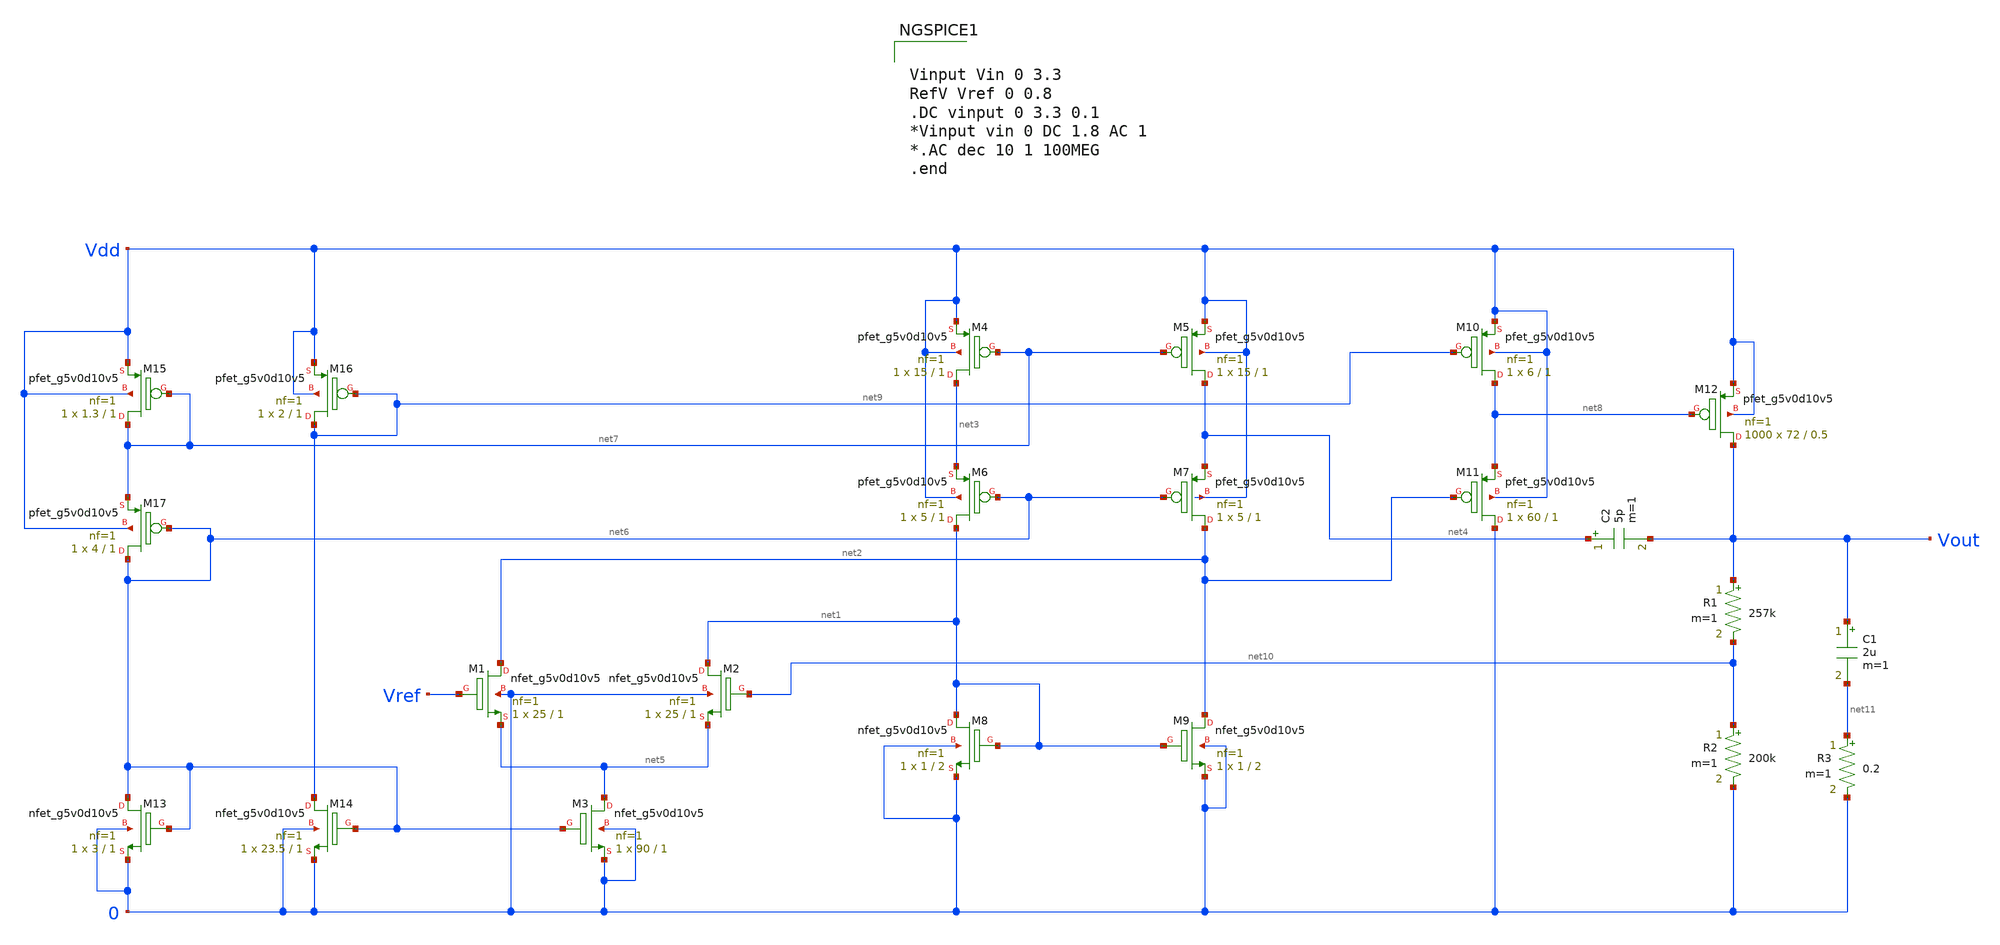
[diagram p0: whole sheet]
** sch_path: LDO/Schematic/LOw_Drop_LDO.sch
**.subckt LOw_Drop_LDO
XM1 net2 Vref net5 0 sky130_fd_pr__nfet_g5v0d10v5 L=1 W=25 nf=1 ad='int((nf+1)/2) * W/nf * 0.29' as='int((nf+2)/2) * W/nf * 0.29'
+ pd='2*int((nf+1)/2) * (W/nf + 0.29)' ps='2*int((nf+2)/2) * (W/nf + 0.29)' nrd='0.29 / W' nrs='0.29 / W'
+ sa=0 sb=0 sd=0 mult=1 m=1
XM2 net1 net10 net5 0 sky130_fd_pr__nfet_g5v0d10v5 L=1 W=25 nf=1 ad='int((nf+1)/2) * W/nf * 0.29' as='int((nf+2)/2) * W/nf * 0.29'
+ pd='2*int((nf+1)/2) * (W/nf + 0.29)' ps='2*int((nf+2)/2) * (W/nf + 0.29)' nrd='0.29 / W' nrs='0.29 / W'
+ sa=0 sb=0 sd=0 mult=1 m=1
XM3 net5 net6 0 0 sky130_fd_pr__nfet_g5v0d10v5 L=1 W=90 nf=1 ad='int((nf+1)/2) * W/nf * 0.29' as='int((nf+2)/2) * W/nf * 0.29'
+ pd='2*int((nf+1)/2) * (W/nf + 0.29)' ps='2*int((nf+2)/2) * (W/nf + 0.29)' nrd='0.29 / W' nrs='0.29 / W'
+ sa=0 sb=0 sd=0 mult=1 m=1
XM4 net3 net7 Vdd Vdd sky130_fd_pr__pfet_g5v0d10v5 L=1 W=15 nf=1 ad='int((nf+1)/2) * W/nf * 0.29' as='int((nf+2)/2) * W/nf * 0.29'
+ pd='2*int((nf+1)/2) * (W/nf + 0.29)' ps='2*int((nf+2)/2) * (W/nf + 0.29)' nrd='0.29 / W' nrs='0.29 / W'
+ sa=0 sb=0 sd=0 mult=1 m=1
XM5 net4 net7 Vdd Vdd sky130_fd_pr__pfet_g5v0d10v5 L=1 W=15 nf=1 ad='int((nf+1)/2) * W/nf * 0.29' as='int((nf+2)/2) * W/nf * 0.29'
+ pd='2*int((nf+1)/2) * (W/nf + 0.29)' ps='2*int((nf+2)/2) * (W/nf + 0.29)' nrd='0.29 / W' nrs='0.29 / W'
+ sa=0 sb=0 sd=0 mult=1 m=1
XM6 net1 net6 net3 Vdd sky130_fd_pr__pfet_g5v0d10v5 L=1 W=5 nf=1 ad='int((nf+1)/2) * W/nf * 0.29' as='int((nf+2)/2) * W/nf * 0.29'
+ pd='2*int((nf+1)/2) * (W/nf + 0.29)' ps='2*int((nf+2)/2) * (W/nf + 0.29)' nrd='0.29 / W' nrs='0.29 / W'
+ sa=0 sb=0 sd=0 mult=1 m=1
XM7 net2 net6 net4 Vdd sky130_fd_pr__pfet_g5v0d10v5 L=1 W=5 nf=1 ad='int((nf+1)/2) * W/nf * 0.29' as='int((nf+2)/2) * W/nf * 0.29'
+ pd='2*int((nf+1)/2) * (W/nf + 0.29)' ps='2*int((nf+2)/2) * (W/nf + 0.29)' nrd='0.29 / W' nrs='0.29 / W'
+ sa=0 sb=0 sd=0 mult=1 m=1
XM8 net1 net1 0 0 sky130_fd_pr__nfet_g5v0d10v5 L=2 W=1 nf=1 ad='int((nf+1)/2) * W/nf * 0.29' as='int((nf+2)/2) * W/nf * 0.29'
+ pd='2*int((nf+1)/2) * (W/nf + 0.29)' ps='2*int((nf+2)/2) * (W/nf + 0.29)' nrd='0.29 / W' nrs='0.29 / W'
+ sa=0 sb=0 sd=0 mult=1 m=1
XM9 net2 net1 0 0 sky130_fd_pr__nfet_g5v0d10v5 L=2 W=1 nf=1 ad='int((nf+1)/2) * W/nf * 0.29' as='int((nf+2)/2) * W/nf * 0.29'
+ pd='2*int((nf+1)/2) * (W/nf + 0.29)' ps='2*int((nf+2)/2) * (W/nf + 0.29)' nrd='0.29 / W' nrs='0.29 / W'
+ sa=0 sb=0 sd=0 mult=1 m=1
XM10 net8 net9 Vdd Vdd sky130_fd_pr__pfet_g5v0d10v5 L=1 W=6 nf=1 ad='int((nf+1)/2) * W/nf * 0.29' as='int((nf+2)/2) * W/nf * 0.29'
+ pd='2*int((nf+1)/2) * (W/nf + 0.29)' ps='2*int((nf+2)/2) * (W/nf + 0.29)' nrd='0.29 / W' nrs='0.29 / W'
+ sa=0 sb=0 sd=0 mult=1 m=1
XM11 0 net2 net8 Vdd sky130_fd_pr__pfet_g5v0d10v5 L=1 W=60 nf=1 ad='int((nf+1)/2) * W/nf * 0.29' as='int((nf+2)/2) * W/nf * 0.29'
+ pd='2*int((nf+1)/2) * (W/nf + 0.29)' ps='2*int((nf+2)/2) * (W/nf + 0.29)' nrd='0.29 / W' nrs='0.29 / W'
+ sa=0 sb=0 sd=0 mult=1 m=1
XM12 Vout net8 Vdd Vdd sky130_fd_pr__pfet_g5v0d10v5 L=0.5 W=72 nf=1 ad='int((nf+1)/2) * W/nf * 0.29'
+ as='int((nf+2)/2) * W/nf * 0.29' pd='2*int((nf+1)/2) * (W/nf + 0.29)' ps='2*int((nf+2)/2) * (W/nf + 0.29)'
+ nrd='0.29 / W' nrs='0.29 / W' sa=0 sb=0 sd=0 mult=1000 m=1000
XM13 net6 net6 0 0 sky130_fd_pr__nfet_g5v0d10v5 L=1 W=3 nf=1 ad='int((nf+1)/2) * W/nf * 0.29' as='int((nf+2)/2) * W/nf * 0.29'
+ pd='2*int((nf+1)/2) * (W/nf + 0.29)' ps='2*int((nf+2)/2) * (W/nf + 0.29)' nrd='0.29 / W' nrs='0.29 / W'
+ sa=0 sb=0 sd=0 mult=1 m=1
XM14 net9 net6 0 0 sky130_fd_pr__nfet_g5v0d10v5 L=1 W=23.5 nf=1 ad='int((nf+1)/2) * W/nf * 0.29' as='int((nf+2)/2) * W/nf * 0.29'
+ pd='2*int((nf+1)/2) * (W/nf + 0.29)' ps='2*int((nf+2)/2) * (W/nf + 0.29)' nrd='0.29 / W' nrs='0.29 / W'
+ sa=0 sb=0 sd=0 mult=1 m=1
XM15 net7 net7 Vdd Vdd sky130_fd_pr__pfet_g5v0d10v5 L=1 W=1.3 nf=1 ad='int((nf+1)/2) * W/nf * 0.29' as='int((nf+2)/2) * W/nf * 0.29'
+ pd='2*int((nf+1)/2) * (W/nf + 0.29)' ps='2*int((nf+2)/2) * (W/nf + 0.29)' nrd='0.29 / W' nrs='0.29 / W'
+ sa=0 sb=0 sd=0 mult=1 m=1
XM16 net9 net9 Vdd Vdd sky130_fd_pr__pfet_g5v0d10v5 L=1 W=2 nf=1 ad='int((nf+1)/2) * W/nf * 0.29' as='int((nf+2)/2) * W/nf * 0.29'
+ pd='2*int((nf+1)/2) * (W/nf + 0.29)' ps='2*int((nf+2)/2) * (W/nf + 0.29)' nrd='0.29 / W' nrs='0.29 / W'
+ sa=0 sb=0 sd=0 mult=1 m=1
XM17 net6 net6 net7 Vdd sky130_fd_pr__pfet_g5v0d10v5 L=1 W=4 nf=1 ad='int((nf+1)/2) * W/nf * 0.29' as='int((nf+2)/2) * W/nf * 0.29'
+ pd='2*int((nf+1)/2) * (W/nf + 0.29)' ps='2*int((nf+2)/2) * (W/nf + 0.29)' nrd='0.29 / W' nrs='0.29 / W'
+ sa=0 sb=0 sd=0 mult=1 m=1
R1 Vout net10 257k m=1
R2 net10 0 200k m=1
R3 net11 0 0.2 m=1
C1 Vout net11 2u m=1
C2 net4 Vout 5p m=1
**** begin user architecture code


Vinput Vin 0 3.3
RefV Vref 0 0.8
.DC vinput 0 3.3 0.1
*Vinput vin 0 DC 1.8 AC 1
*.AC dec 10 1 100MEG
.end



.include $::SKYWATER_MODELS/cells/nfet_01v8/sky130_fd_pr__nfet_01v8__tt.corner.spice
.include $::SKYWATER_MODELS/cells/nfet_01v8_lvt/sky130_fd_pr__nfet_01v8_lvt__tt.corner.spice
.include $::SKYWATER_MODELS/cells/pfet_01v8/sky130_fd_pr__pfet_01v8__tt.corner.spice
.include $::SKYWATER_MODELS/cells/nfet_03v3_nvt/sky130_fd_pr__nfet_03v3_nvt__tt.corner.spice
.include $::SKYWATER_MODELS/cells/nfet_05v0_nvt/sky130_fd_pr__nfet_05v0_nvt__tt.corner.spice
.include $::SKYWATER_MODELS/cells/esd_nfet_01v8/sky130_fd_pr__esd_nfet_01v8__tt.corner.spice
.include $::SKYWATER_MODELS/cells/pfet_01v8_lvt/sky130_fd_pr__pfet_01v8_lvt__tt.corner.spice
.include $::SKYWATER_MODELS/cells/pfet_01v8_hvt/sky130_fd_pr__pfet_01v8_hvt__tt.corner.spice
.include $::SKYWATER_MODELS/cells/esd_pfet_g5v0d10v5/sky130_fd_pr__esd_pfet_g5v0d10v5__tt.corner.spice
.include $::SKYWATER_MODELS/cells/pfet_g5v0d10v5/sky130_fd_pr__pfet_g5v0d10v5__tt.corner.spice
.include $::SKYWATER_MODELS/cells/pfet_g5v0d16v0/sky130_fd_pr__pfet_g5v0d16v0__tt.corner.spice
.include $::SKYWATER_MODELS/cells/nfet_g5v0d10v5/sky130_fd_pr__nfet_g5v0d10v5__tt.corner.spice
.include $::SKYWATER_MODELS/cells/nfet_g5v0d16v0/sky130_fd_pr__nfet_g5v0d16v0__tt_discrete.corner.spice
.include $::SKYWATER_MODELS/cells/esd_nfet_g5v0d10v5/sky130_fd_pr__esd_nfet_g5v0d10v5__tt.corner.spice
.include $::SKYWATER_MODELS/models/corners/tt/nonfet.spice
* Mismatch parameters
.include $::SKYWATER_MODELS/cells/nfet_01v8/sky130_fd_pr__nfet_01v8__mismatch.corner.spice
.include $::SKYWATER_MODELS/cells/pfet_01v8/sky130_fd_pr__pfet_01v8__mismatch.corner.spice
.include $::SKYWATER_MODELS/cells/nfet_01v8_lvt/sky130_fd_pr__nfet_01v8_lvt__mismatch.corner.spice
.include $::SKYWATER_MODELS/cells/pfet_01v8_lvt/sky130_fd_pr__pfet_01v8_lvt__mismatch.corner.spice
.include $::SKYWATER_MODELS/cells/pfet_01v8_hvt/sky130_fd_pr__pfet_01v8_hvt__mismatch.corner.spice
.include $::SKYWATER_MODELS/cells/nfet_g5v0d10v5/sky130_fd_pr__nfet_g5v0d10v5__mismatch.corner.spice
.include $::SKYWATER_MODELS/cells/pfet_g5v0d10v5/sky130_fd_pr__pfet_g5v0d10v5__mismatch.corner.spice
.include $::SKYWATER_MODELS/cells/nfet_05v0_nvt/sky130_fd_pr__nfet_05v0_nvt__mismatch.corner.spice
.include $::SKYWATER_MODELS/cells/nfet_03v3_nvt/sky130_fd_pr__nfet_03v3_nvt__mismatch.corner.spice
* Resistor$::SKYWATER_MODELS/Capacitor
.include $::SKYWATER_MODELS/models/r+c/res_typical__cap_typical.spice
.include $::SKYWATER_MODELS/models/r+c/res_typical__cap_typical__lin.spice
* Special cells
.include $::SKYWATER_MODELS/models/corners/tt/specialized_cells.spice
* All models
.include $::SKYWATER_MODELS/models/all.spice
* Corner
.include $::SKYWATER_MODELS/models/corners/tt/rf.spice

**** end user architecture code
**.ends
.end
